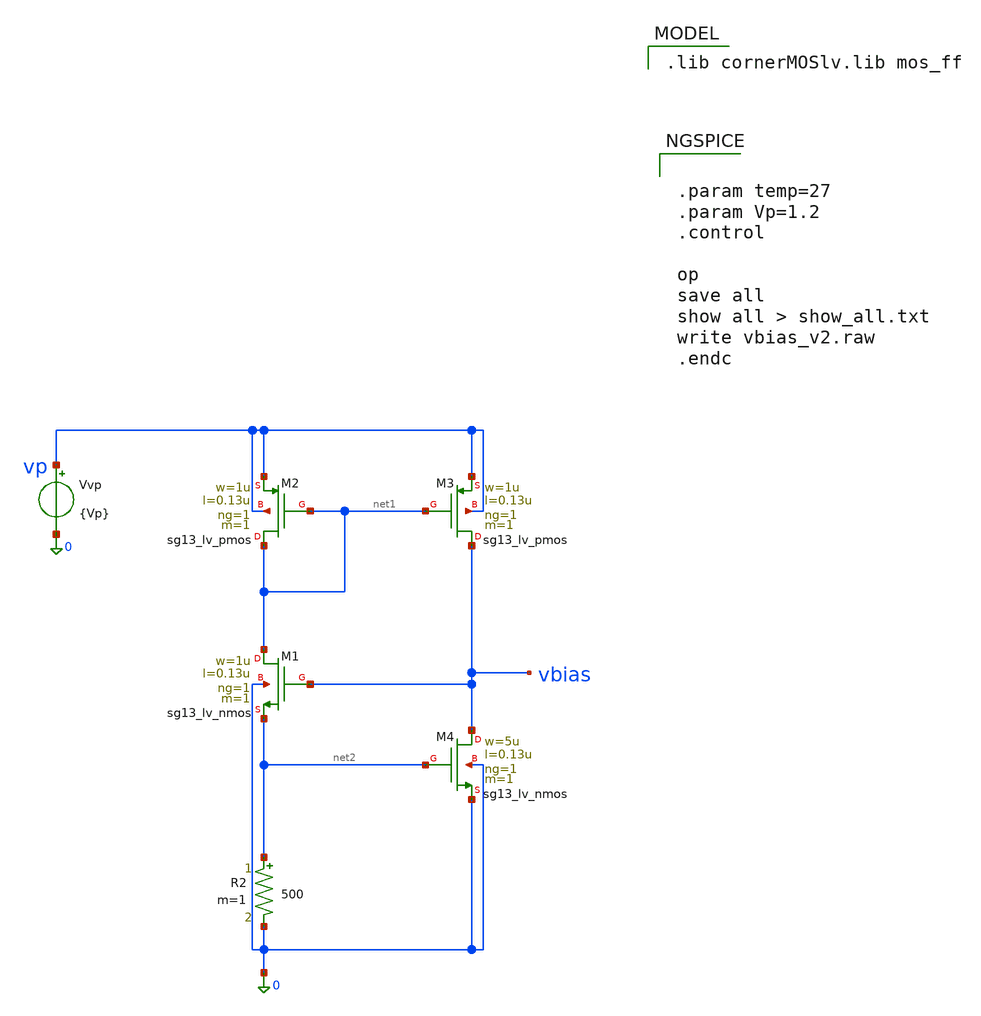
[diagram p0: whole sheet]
** sch_path: schematics/charge_pump/old_sch/vbias_v3.sch
**.subckt vbias_v3
XM1 net1 vbias net2 0 sg13_lv_nmos w=1u l=0.13u ng=1 m=1 mm_ok=1
XM2 net1 net1 vp vp sg13_lv_pmos w=1u l=0.13u ng=1 m=1 mm_ok=1
XM3 vbias net1 vp vp sg13_lv_pmos w=1u l=0.13u ng=1 m=1 mm_ok=1
XM4 vbias net2 0 0 sg13_lv_nmos w=5u l=0.13u ng=1 m=1 mm_ok=1
R2 net2 0 500 m=1
Vvp vp 0 {Vp}
**** begin user architecture code
 .lib cornerMOSlv.lib mos_ff



.param temp=27
.param Vp=1.2
.control

op
save all
show all > show_all.txt
write vbias_v2.raw
.endc


**** end user architecture code
**.ends
.end
